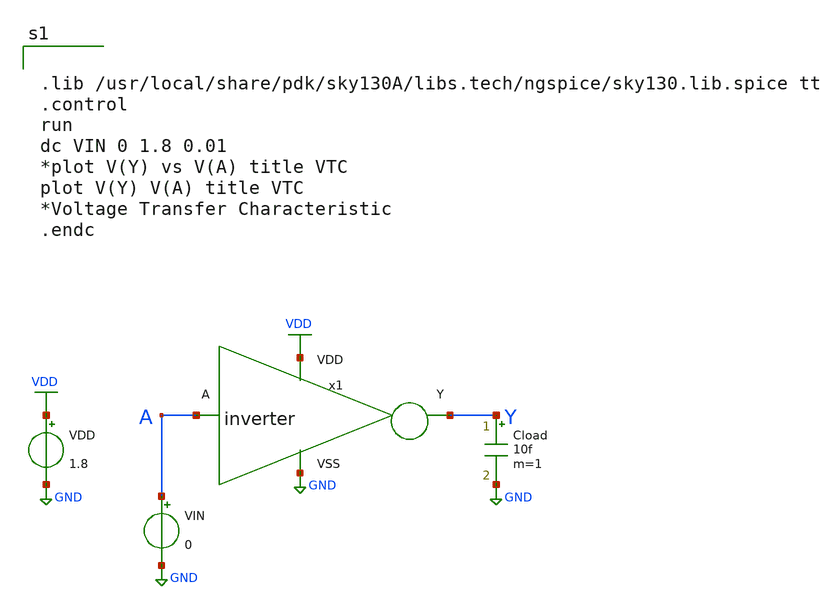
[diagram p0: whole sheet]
** sch_path: inverter/design_circuit/dc_inverter.sch
**.subckt dc_inverter
VIN A GND 0
x1 A Y VDD GND inverter
Cload Y GND 10f m=1
VDD VDD GND 1.8
**** begin user architecture code


.lib /usr/local/share/pdk/sky130A/libs.tech/ngspice/sky130.lib.spice tt
.control
run
dc VIN 0 1.8 0.01
*plot V(Y) vs V(A) title VTC
plot V(Y) V(A) title VTC
*Voltage Transfer Characteristic
.endc


**** end user architecture code
**.ends
.GLOBAL GND
.GLOBAL VDD
.end
